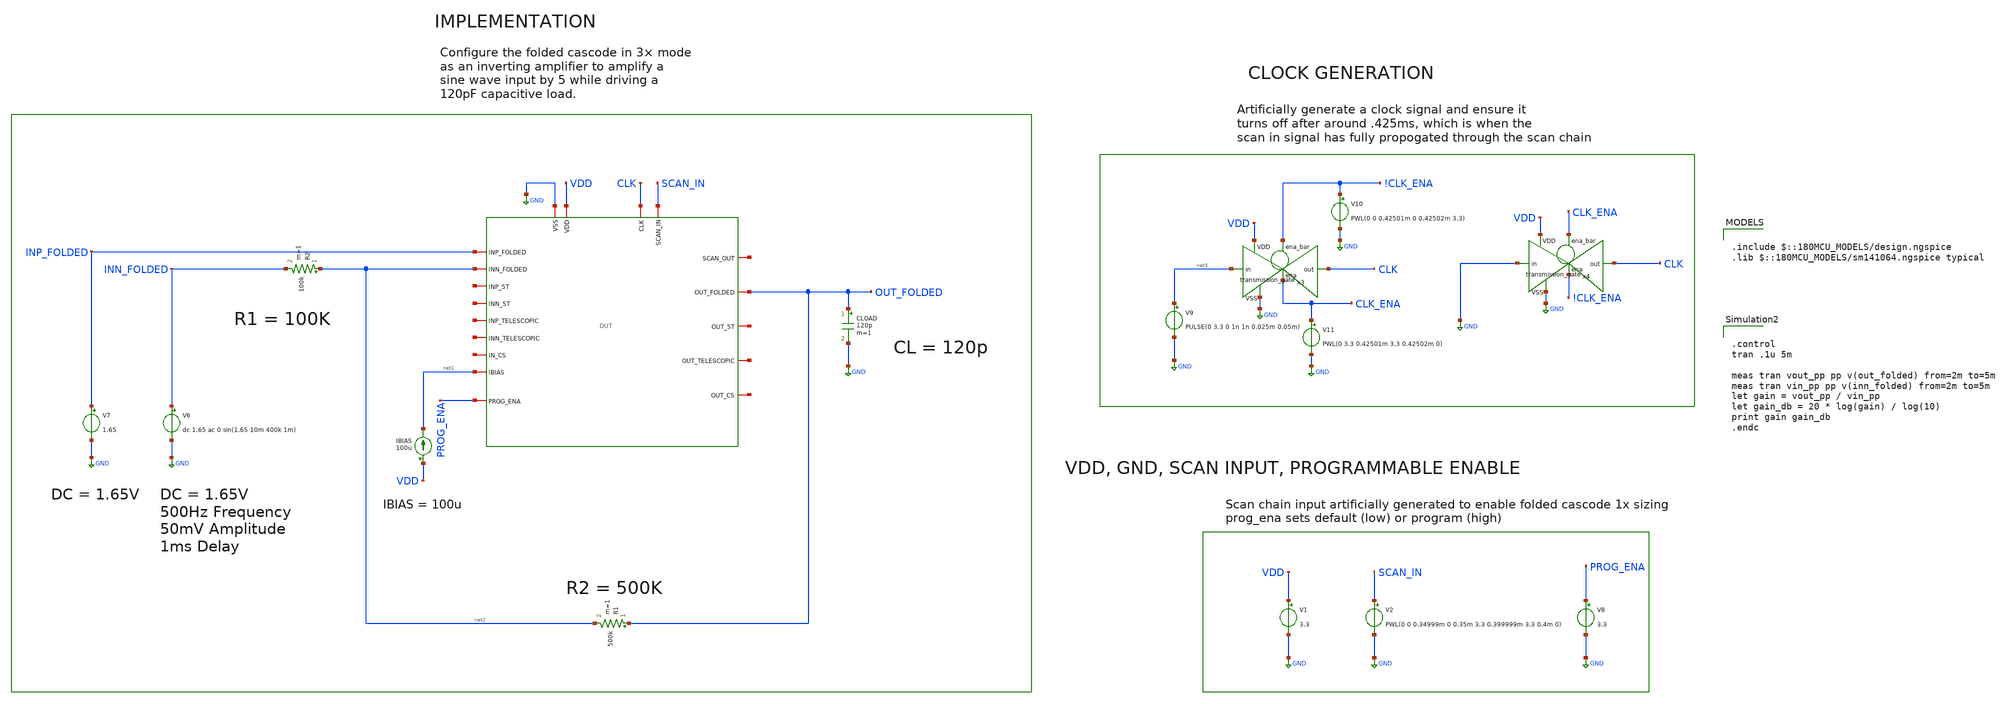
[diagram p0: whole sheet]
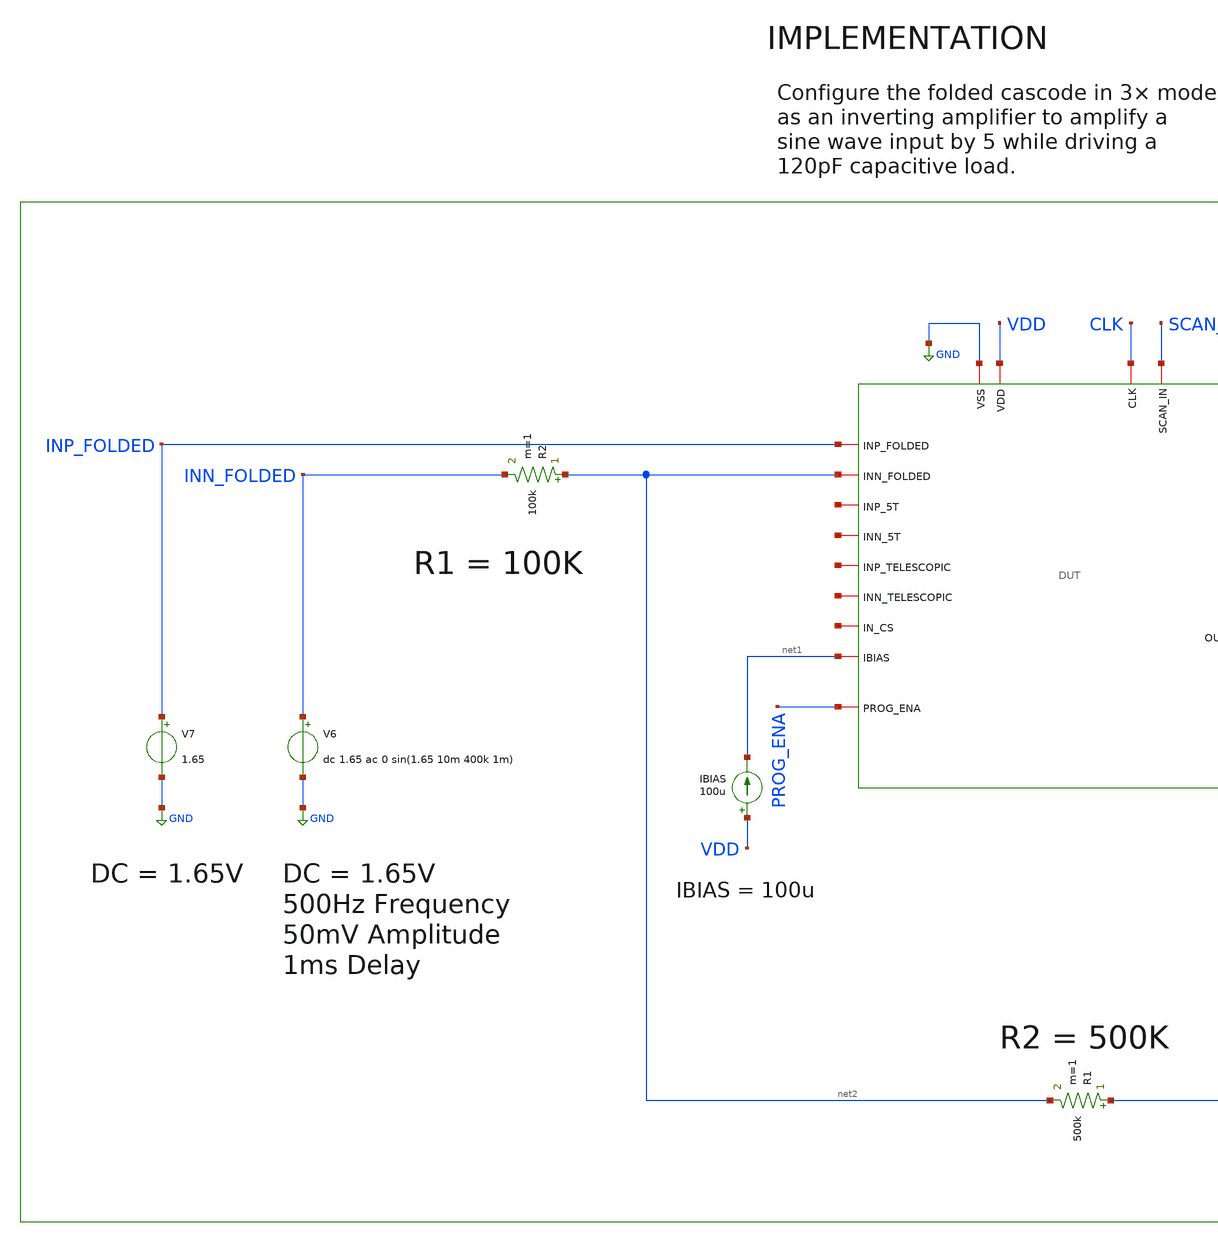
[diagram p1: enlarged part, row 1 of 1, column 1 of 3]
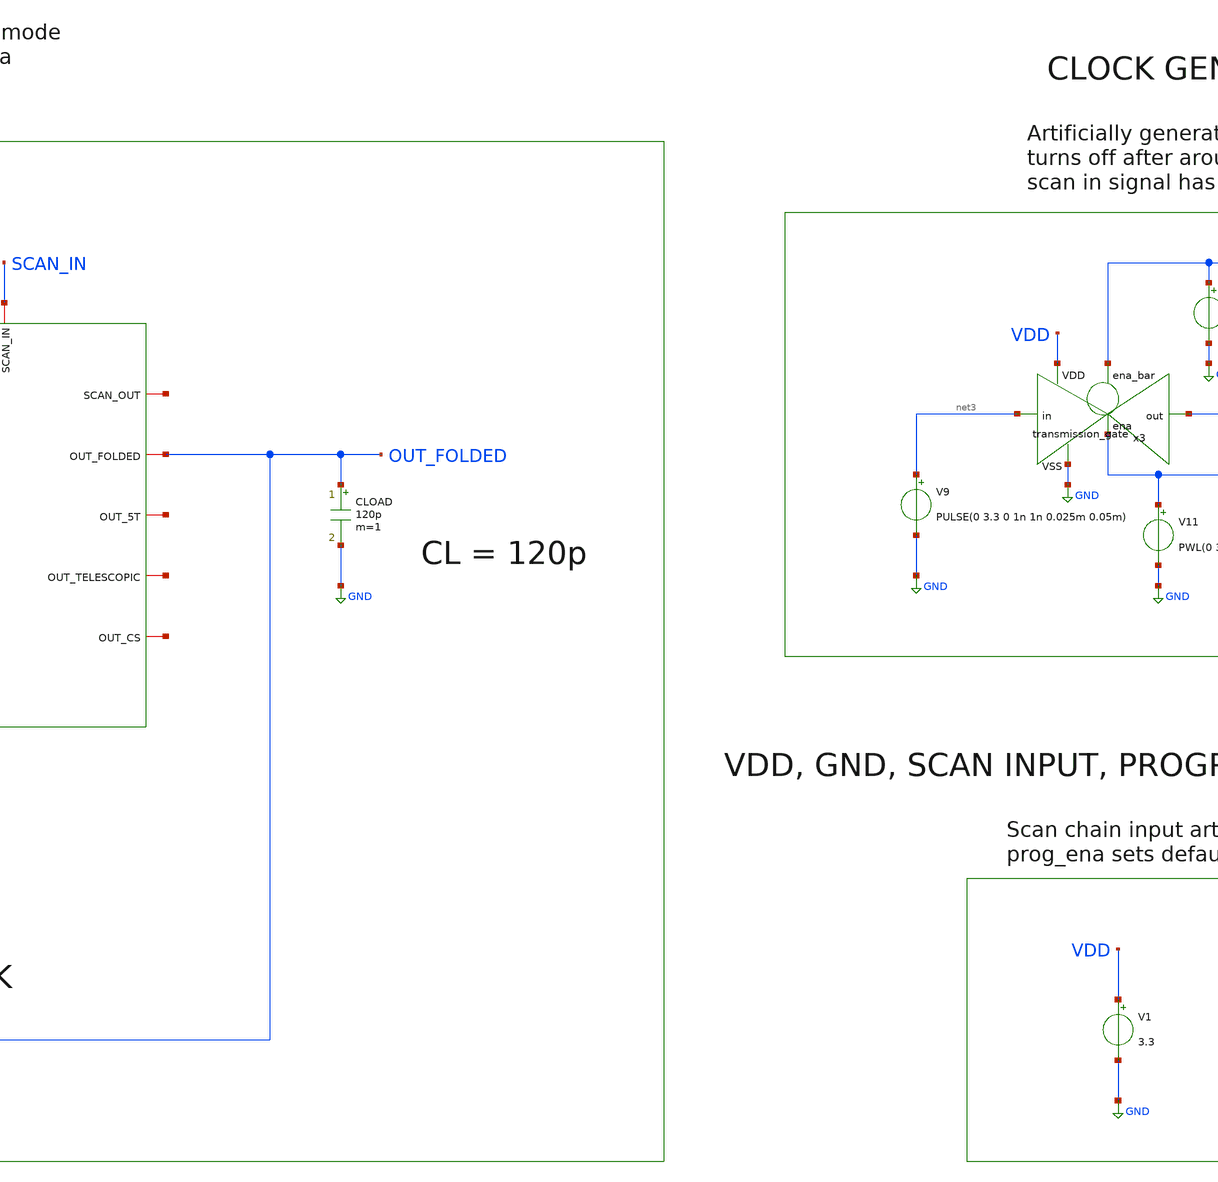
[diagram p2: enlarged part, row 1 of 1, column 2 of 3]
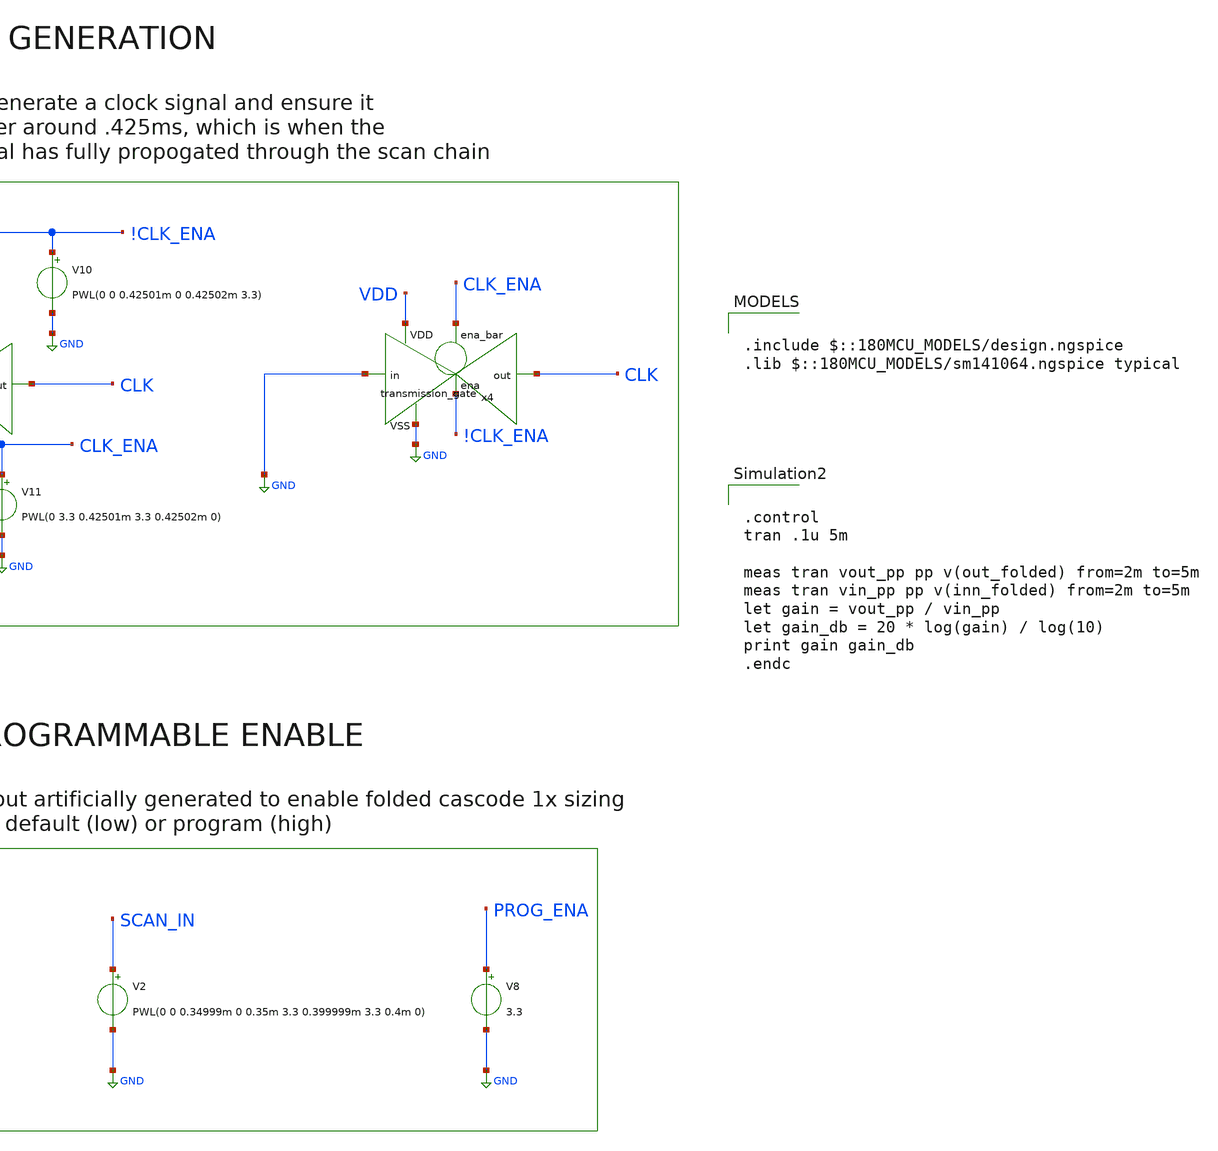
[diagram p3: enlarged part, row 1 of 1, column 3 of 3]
** sch_path: designs/libs/verification/ota_folded/3x_sizing/bandwidth_tb.sch
**.subckt bandwidth_tb
V1 VDD GND 3.3
IBIAS VDD net1 100u
V7 INP_FOLDED GND 1.65
CLOAD OUT_FOLDED GND 120p m=1
R2 net2 INN_FOLDED 100k m=1
V6 INN_FOLDED GND dc 1.65 ac 0 sin(1.65 10m 400k 1m)
R1 OUT_FOLDED net2 500k m=1
x1 CLK net4 SCAN_IN GND VDD OUT_FOLDED INP_FOLDED net5 net1 net2 net6 net7 net8 net9 net10 net11
+ net12 PROG_ENA DUT
V8 PROG_ENA GND 3.3
V9 net3 GND PULSE(0 3.3 0 1n 1n 0.025m 0.05m)
x3 !CLK_ENA VDD CLK net3 GND CLK_ENA transmission_gate
V10 !CLK_ENA GND PWL(0 0 0.42501m 0 0.42502m 3.3)
V11 CLK_ENA GND PWL(0 3.3 0.42501m 3.3 0.42502m 0)
x4 CLK_ENA VDD CLK GND GND !CLK_ENA transmission_gate
V2 SCAN_IN GND PWL(0 0 0.34999m 0 0.35m 3.3 0.399999m 3.3 0.4m 0)
**** begin user architecture code

.include $::180MCU_MODELS/design.ngspice
.lib $::180MCU_MODELS/sm141064.ngspice typical



.control
tran .1u 5m

meas tran vout_pp pp v(out_folded) from=2m to=5m
meas tran vin_pp pp v(inn_folded) from=2m to=5m
let gain = vout_pp / vin_pp
let gain_db = 20 * log(gain) / log(10)
print gain gain_db
.endc


**** end user architecture code
**.ends
.GLOBAL GND
.end
